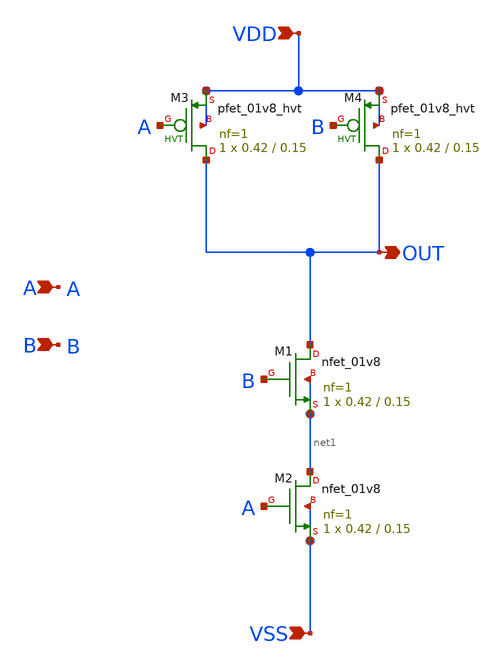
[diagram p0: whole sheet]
** sch_path: design/LELO_SVOD_SKY130A/LELO_NAND.sch
**.subckt LELO_NAND VDD VSS OUT A B
*.ipin VDD
*.ipin VSS
*.opin OUT
*.ipin A
*.ipin B
XM1 OUT B net1 net1 sky130_fd_pr__nfet_01v8 L=0.15 W=0.42 nf=1 ad='int((1 + 1)/2) * 0.42 / 1 * 0.29'
+ as='int((1 + 2)/2) * 0.42 / 1 * 0.29' pd='2*int((1 + 1)/2) * (0.42 / 1 + 0.29)' ps='2*int((1 + 2)/2) * (0.42 / 1 + 0.29)'
+ nrd='0.29 / 0.42 ' nrs='0.29 / 0.42 ' sa=0 sb=0 sd=0 mult=1 m=1
XM2 net1 A VSS VSS sky130_fd_pr__nfet_01v8 L=0.15 W=0.42 nf=1 ad='int((1 + 1)/2) * 0.42 / 1 * 0.29' as='int((1 + 2)/2) * 0.42 / 1 * 0.29'
+ pd='2*int((1 + 1)/2) * (0.42 / 1 + 0.29)' ps='2*int((1 + 2)/2) * (0.42 / 1 + 0.29)' nrd='0.29 / 0.42 '
+ nrs='0.29 / 0.42 ' sa=0 sb=0 sd=0 mult=1 m=1
XM3 OUT A VDD VDD sky130_fd_pr__pfet_01v8_hvt L=0.15 W=0.42 nf=1 ad='int((1 + 1)/2) * 0.42 / 1 * 0.29'
+ as='int((1 + 2)/2) * 0.42 / 1 * 0.29' pd='2*int((1 + 1)/2) * (0.42 / 1 + 0.29)' ps='2*int((1 + 2)/2) * (0.42 / 1 + 0.29)'
+ nrd='0.29 / 0.42 ' nrs='0.29 / 0.42 ' sa=0 sb=0 sd=0 mult=1 m=1
XM4 OUT B VDD VDD sky130_fd_pr__pfet_01v8_hvt L=0.15 W=0.42 nf=1 ad='int((1 + 1)/2) * 0.42 / 1 * 0.29'
+ as='int((1 + 2)/2) * 0.42 / 1 * 0.29' pd='2*int((1 + 1)/2) * (0.42 / 1 + 0.29)' ps='2*int((1 + 2)/2) * (0.42 / 1 + 0.29)'
+ nrd='0.29 / 0.42 ' nrs='0.29 / 0.42 ' sa=0 sb=0 sd=0 mult=1 m=1
**.ends
.end
